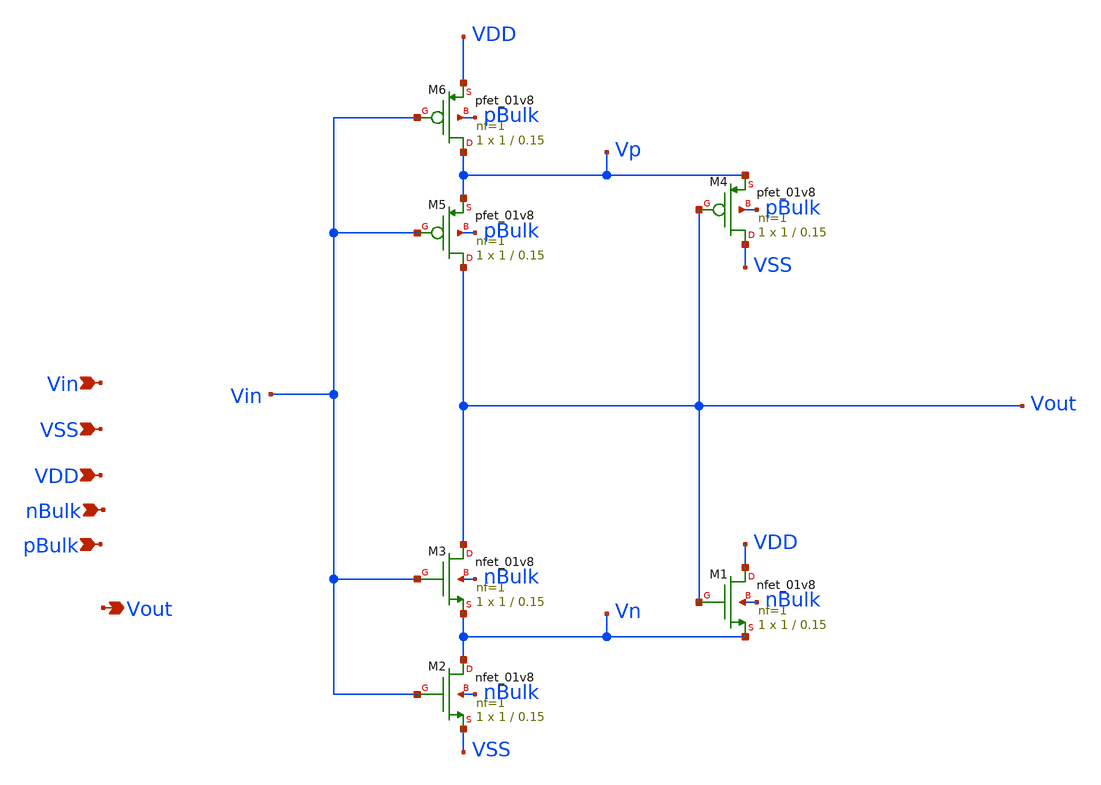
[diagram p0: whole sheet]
** sch_path: tt10-hdl/tt_um_test_commit/xschem/T1/schmTrigg/schmTrigg.sch
**.subckt schmTrigg Vin VDD VSS Vout nBulk pBulk
*.ipin Vin
*.ipin VDD
*.ipin VSS
*.opin Vout
*.ipin nBulk
*.ipin pBulk
XM1 VDD Vout Vn nBulk sky130_fd_pr__nfet_01v8 L=0.15 W=1 nf=1 ad='int((1 + 1)/2) * 1 / 1 * 0.29' as='int((1 + 2)/2) * 1 / 1 * 0.29'
+ pd='2*int((1 + 1)/2) * (1 / 1 + 0.29)' ps='2*int((1 + 2)/2) * (1 / 1 + 0.29)' nrd='0.29 / 1 ' nrs='0.29 / 1 '
+ sa=0 sb=0 sd=0 mult=1 m=1
XM2 Vn Vin VSS nBulk sky130_fd_pr__nfet_01v8 L=0.15 W=1 nf=1 ad='int((1 + 1)/2) * 1 / 1 * 0.29' as='int((1 + 2)/2) * 1 / 1 * 0.29'
+ pd='2*int((1 + 1)/2) * (1 / 1 + 0.29)' ps='2*int((1 + 2)/2) * (1 / 1 + 0.29)' nrd='0.29 / 1 ' nrs='0.29 / 1 '
+ sa=0 sb=0 sd=0 mult=1 m=1
XM3 Vout Vin Vn nBulk sky130_fd_pr__nfet_01v8 L=0.15 W=1 nf=1 ad='int((1 + 1)/2) * 1 / 1 * 0.29' as='int((1 + 2)/2) * 1 / 1 * 0.29'
+ pd='2*int((1 + 1)/2) * (1 / 1 + 0.29)' ps='2*int((1 + 2)/2) * (1 / 1 + 0.29)' nrd='0.29 / 1 ' nrs='0.29 / 1 '
+ sa=0 sb=0 sd=0 mult=1 m=1
XM4 VSS Vout Vp pBulk sky130_fd_pr__pfet_01v8 L=0.15 W=1 nf=1 ad='int((nf+1)/2) * W/nf * 0.29' as='int((nf+2)/2) * W/nf * 0.29'
+ pd='2*int((nf+1)/2) * (W/nf + 0.29)' ps='2*int((nf+2)/2) * (W/nf + 0.29)' nrd='0.29 / W' nrs='0.29 / W'
+ sa=0 sb=0 sd=0 mult=1 m=1
XM5 Vout Vin Vp pBulk sky130_fd_pr__pfet_01v8 L=0.15 W=1 nf=1 ad='int((nf+1)/2) * W/nf * 0.29' as='int((nf+2)/2) * W/nf * 0.29'
+ pd='2*int((nf+1)/2) * (W/nf + 0.29)' ps='2*int((nf+2)/2) * (W/nf + 0.29)' nrd='0.29 / W' nrs='0.29 / W'
+ sa=0 sb=0 sd=0 mult=1 m=1
XM6 Vp Vin VDD pBulk sky130_fd_pr__pfet_01v8 L=0.15 W=1 nf=1 ad='int((nf+1)/2) * W/nf * 0.29' as='int((nf+2)/2) * W/nf * 0.29'
+ pd='2*int((nf+1)/2) * (W/nf + 0.29)' ps='2*int((nf+2)/2) * (W/nf + 0.29)' nrd='0.29 / W' nrs='0.29 / W'
+ sa=0 sb=0 sd=0 mult=1 m=1
**.ends
.end
